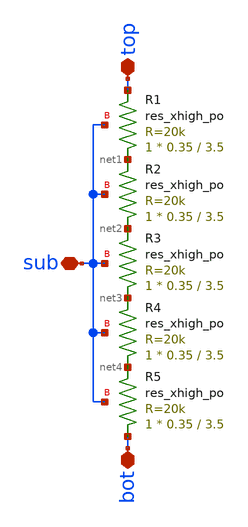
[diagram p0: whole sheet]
** sch_path: xschem/res100k.sch
**.subckt res100k top bot sub
*.iopin top
*.iopin bot
*.iopin sub
XR1 net1 top sub sky130_fd_pr__res_xhigh_po W=0.35 L=3.5 mult=1 m=1
XR2 net2 net1 sub sky130_fd_pr__res_xhigh_po W=0.35 L=3.5 mult=1 m=1
XR3 net3 net2 sub sky130_fd_pr__res_xhigh_po W=0.35 L=3.5 mult=1 m=1
XR4 net4 net3 sub sky130_fd_pr__res_xhigh_po W=0.35 L=3.5 mult=1 m=1
XR5 bot net4 sub sky130_fd_pr__res_xhigh_po W=0.35 L=3.5 mult=1 m=1
**.ends
.end
